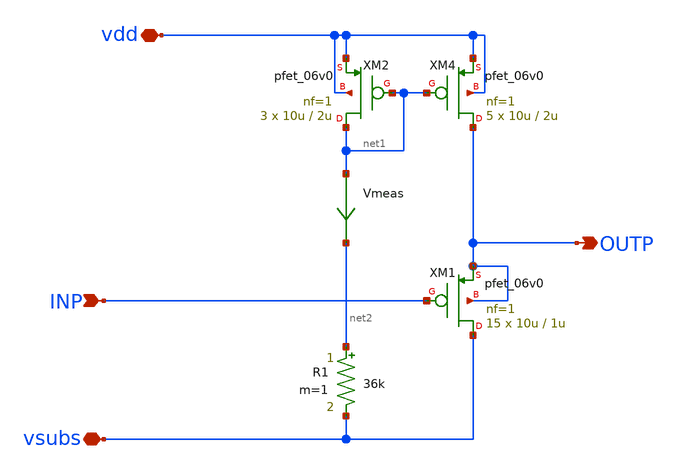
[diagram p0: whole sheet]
** sch_path: xschem/ip_buffer.sch
**.subckt ip_buffer vsubs vdd INP OUTP
*.iopin vsubs
*.iopin vdd
*.ipin INP
*.opin OUTP
XM1 vsubs INP OUTP OUTP pfet_06v0 L=1u W=10u nf=1 ad='int((nf+1)/2) * W/nf * 0.18u' as='int((nf+2)/2) * W/nf * 0.18u'
+ pd='2*int((nf+1)/2) * (W/nf + 0.18u)' ps='2*int((nf+2)/2) * (W/nf + 0.18u)' nrd='0.18u / W' nrs='0.18u / W'
+ sa=0 sb=0 sd=0 m=15
R1 net2 vsubs 36k m=1
Vmeas net1 net2 0
XM4 OUTP net1 vdd vdd pfet_06v0 L=2u W=10u nf=1 ad='int((nf+1)/2) * W/nf * 0.18u' as='int((nf+2)/2) * W/nf * 0.18u'
+ pd='2*int((nf+1)/2) * (W/nf + 0.18u)' ps='2*int((nf+2)/2) * (W/nf + 0.18u)' nrd='0.18u / W' nrs='0.18u / W'
+ sa=0 sb=0 sd=0 m=5
XM2 net1 net1 vdd vdd pfet_06v0 L=2u W=10u nf=1 ad='int((nf+1)/2) * W/nf * 0.18u' as='int((nf+2)/2) * W/nf * 0.18u'
+ pd='2*int((nf+1)/2) * (W/nf + 0.18u)' ps='2*int((nf+2)/2) * (W/nf + 0.18u)' nrd='0.18u / W' nrs='0.18u / W'
+ sa=0 sb=0 sd=0 m=3
**.ends
.end
